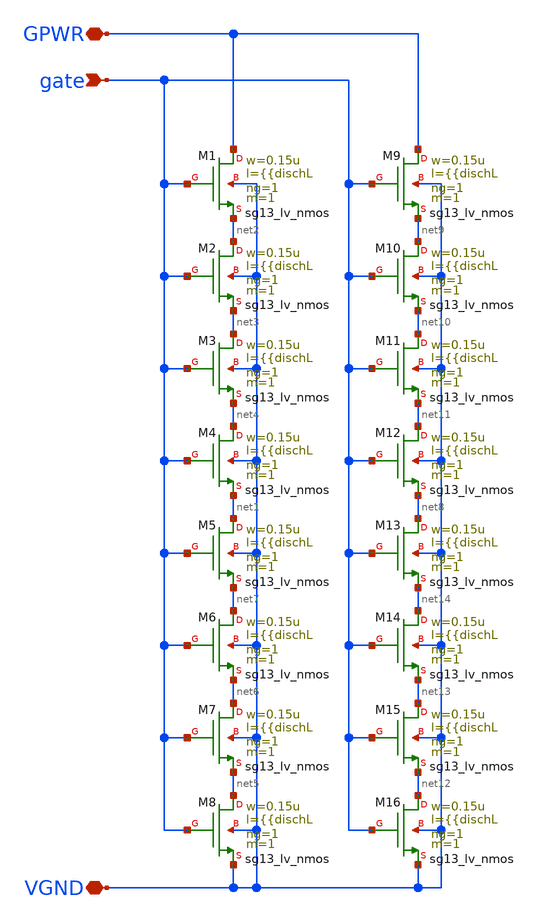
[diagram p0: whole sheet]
** sch_path: ihp-sg13cmos5l/libs.tech/generators/hm_pg/hm_pg_lv/xschem/dischg.sch
**.subckt dischg GPWR VGND gate
*.iopin GPWR
*.iopin VGND
*.ipin gate
XM1 GPWR gate net2 VGND sg13_lv_nmos w=0.15u l={{dischL ng=1 m=1 mm_ok=1
XM2 net2 gate net3 VGND sg13_lv_nmos w=0.15u l={{dischL ng=1 m=1 mm_ok=1
XM3 net3 gate net4 VGND sg13_lv_nmos w=0.15u l={{dischL ng=1 m=1 mm_ok=1
XM4 net4 gate net1 VGND sg13_lv_nmos w=0.15u l={{dischL ng=1 m=1 mm_ok=1
XM5 net1 gate net7 VGND sg13_lv_nmos w=0.15u l={{dischL ng=1 m=1 mm_ok=1
XM6 net7 gate net6 VGND sg13_lv_nmos w=0.15u l={{dischL ng=1 m=1 mm_ok=1
XM7 net6 gate net5 VGND sg13_lv_nmos w=0.15u l={{dischL ng=1 m=1 mm_ok=1
XM8 net5 gate VGND VGND sg13_lv_nmos w=0.15u l={{dischL ng=1 m=1 mm_ok=1
XM9 GPWR gate net9 VGND sg13_lv_nmos w=0.15u l={{dischL ng=1 m=1 mm_ok=1
XM10 net9 gate net10 VGND sg13_lv_nmos w=0.15u l={{dischL ng=1 m=1 mm_ok=1
XM11 net10 gate net11 VGND sg13_lv_nmos w=0.15u l={{dischL ng=1 m=1 mm_ok=1
XM12 net11 gate net8 VGND sg13_lv_nmos w=0.15u l={{dischL ng=1 m=1 mm_ok=1
XM13 net8 gate net14 VGND sg13_lv_nmos w=0.15u l={{dischL ng=1 m=1 mm_ok=1
XM14 net14 gate net13 VGND sg13_lv_nmos w=0.15u l={{dischL ng=1 m=1 mm_ok=1
XM15 net13 gate net12 VGND sg13_lv_nmos w=0.15u l={{dischL ng=1 m=1 mm_ok=1
XM16 net12 gate VGND VGND sg13_lv_nmos w=0.15u l={{dischL ng=1 m=1 mm_ok=1
**.ends
.end
